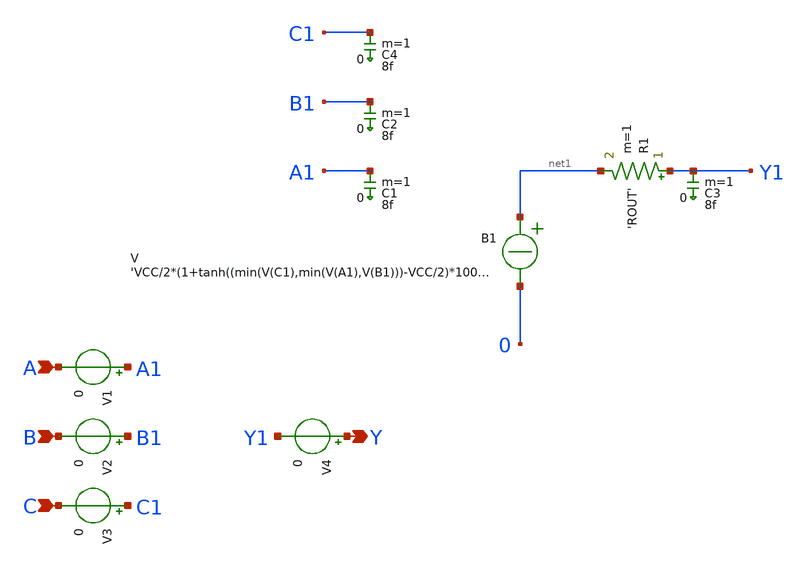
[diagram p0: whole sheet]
** sch_path: xschem_libs_newsym/ngspice/and3_ngspice/schematic/and3_ngspice.sch
* Copyright (C) 1998-2024 Stefan Frederik Schippers
* This program is free software; you can redistribute it and/or modify
* it under the terms of the GNU General Public License as published by
* the Free Software Foundation; either version 2 of the License, or
* (at your option) any later version.
* This program is distributed in the hope that it will be useful,
* but WITHOUT ANY WARRANTY; without even the implied warranty of
* MERCHANTABILITY or FITNESS FOR A PARTICULAR PURPOSE.  See the
* GNU General Public License for more details.
* You should have received a copy of the GNU General Public License
* along with this program; if not, write to the Free Software
**.subckt and3_ngspice A Y B C
*.ipin A
*.opin Y
*.ipin B
*.ipin C
B1 net1 0 V = 'VCC/2*(1+tanh((min(V(C1),min(V(A1),V(B1)))-VCC/2)*100))'
R1 Y1 net1 'ROUT' m=1
C1 A1 0 8f m=1
C2 B1 0 8f m=1
C3 Y1 0 8f m=1
C4 C1 0 8f m=1
V1 A1 A 0
V2 B1 B 0
V3 C1 C 0
V4 Y Y1 0
**.ends
.end
